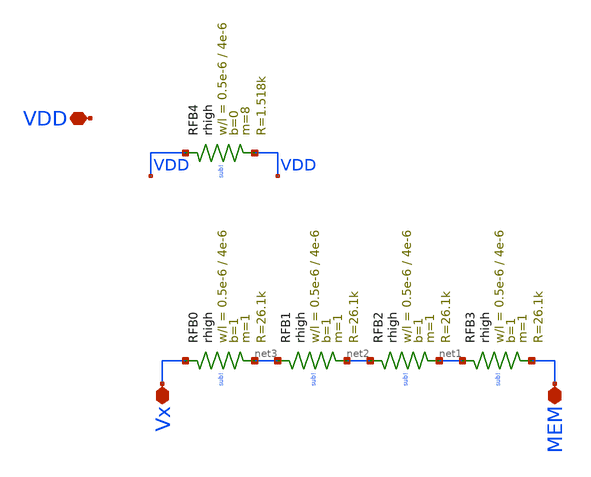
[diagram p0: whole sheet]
** sch_path: work/resistance_bench/resistence_bench.sch
**.subckt resistence_bench VDD Vx MEM
*.iopin VDD
*.iopin Vx
*.iopin MEM
XRFB0 Vx net3 sub! rhigh w=0.5e-6 l=4e-6 m=1 b=1 mm_ok=1
XRFB4 VDD VDD sub! rhigh w=0.5e-6 l=4e-6 m=8 b=0 mm_ok=1
XRFB1 net3 net2 sub! rhigh w=0.5e-6 l=4e-6 m=1 b=1 mm_ok=1
XRFB2 net2 net1 sub! rhigh w=0.5e-6 l=4e-6 m=1 b=1 mm_ok=1
XRFB3 net1 MEM sub! rhigh w=0.5e-6 l=4e-6 m=1 b=1 mm_ok=1
**.ends
.end
